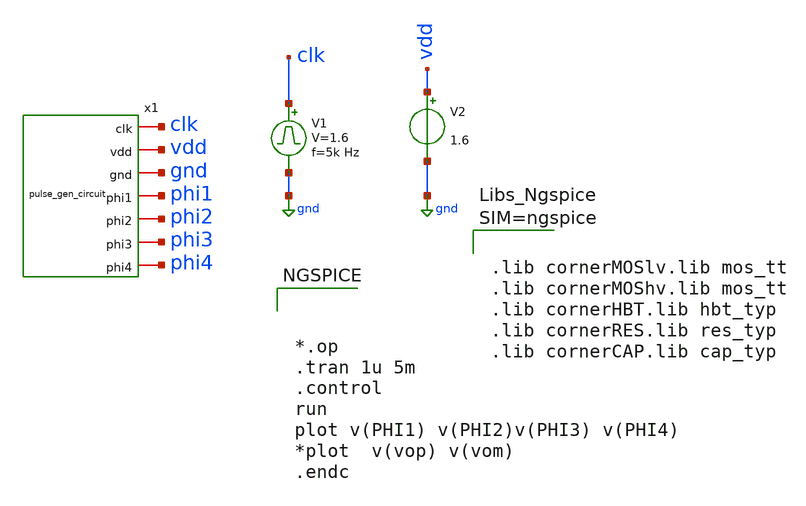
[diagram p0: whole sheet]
** sch_path: dependencies/OTA/OTA-main/schematic/xschem/test.sch
**.subckt test
V2 vdd gnd 1.6
V1 clk gnd pulse 0 1.6 '0.495/ 5k ' '0.01/5k ' '0.01/5k ' '0.49/5k ' '1/5k '
x1 clk vdd gnd phi1 phi2 phi3 phi4 pulse_gen_circuit
**** begin user architecture code



*.op
.tran 1u 5m
.control
run
plot v(PHI1) v(PHI2)v(PHI3) v(PHI4)
*plot  v(vop) v(vom)
.endc





.lib cornerMOSlv.lib mos_tt
.lib cornerMOShv.lib mos_tt
.lib cornerHBT.lib hbt_typ
.lib cornerRES.lib res_typ
.lib cornerCAP.lib cap_typ



**** end user architecture code
**.ends
.GLOBAL gnd
.end
